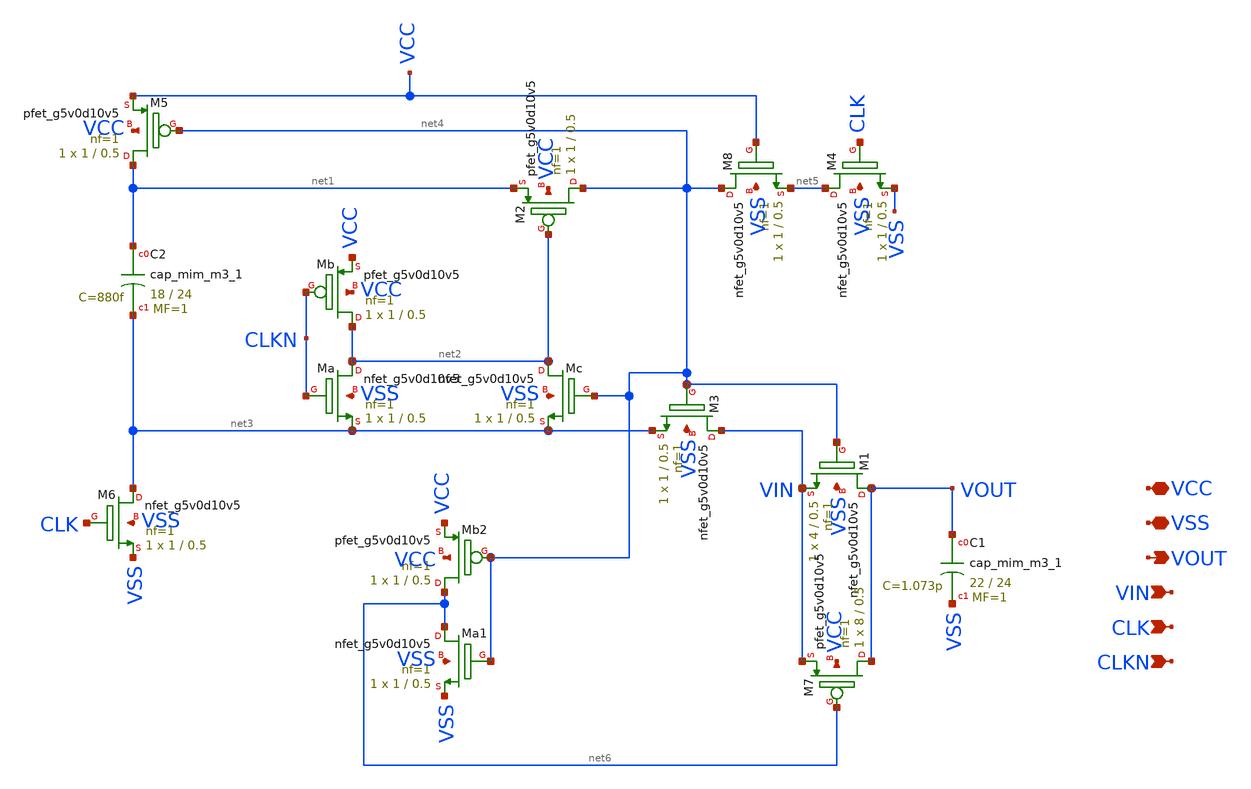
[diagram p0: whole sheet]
** sch_path: Sample&Hold/schematic/working/sample_hold.sch
**.subckt sample_hold VCC VIN VOUT CLK CLKN VSS
*.iopin VCC
*.ipin VIN
*.opin VOUT
*.ipin CLK
*.ipin CLKN
*.iopin VSS
XM5 net1 net4 VCC VCC sky130_fd_pr__pfet_g5v0d10v5 L=0.5 W=1 nf=1 ad='int((nf+1)/2) * W/nf * 0.29' as='int((nf+2)/2) * W/nf * 0.29'
+ pd='2*int((nf+1)/2) * (W/nf + 0.29)' ps='2*int((nf+2)/2) * (W/nf + 0.29)' nrd='0.29 / W' nrs='0.29 / W'
+ sa=0 sb=0 sd=0 mult=1 m=1
XM6 net3 CLK VSS VSS sky130_fd_pr__nfet_g5v0d10v5 L=0.5 W=1 nf=1 ad='int((nf+1)/2) * W/nf * 0.29' as='int((nf+2)/2) * W/nf * 0.29'
+ pd='2*int((nf+1)/2) * (W/nf + 0.29)' ps='2*int((nf+2)/2) * (W/nf + 0.29)' nrd='0.29 / W' nrs='0.29 / W'
+ sa=0 sb=0 sd=0 mult=1 m=1
XMa net2 CLKN net3 VSS sky130_fd_pr__nfet_g5v0d10v5 L=0.5 W=1 nf=1 ad='int((nf+1)/2) * W/nf * 0.29' as='int((nf+2)/2) * W/nf * 0.29'
+ pd='2*int((nf+1)/2) * (W/nf + 0.29)' ps='2*int((nf+2)/2) * (W/nf + 0.29)' nrd='0.29 / W' nrs='0.29 / W'
+ sa=0 sb=0 sd=0 mult=1 m=1
XMb net2 CLKN VCC VCC sky130_fd_pr__pfet_g5v0d10v5 L=0.5 W=1 nf=1 ad='int((nf+1)/2) * W/nf * 0.29' as='int((nf+2)/2) * W/nf * 0.29'
+ pd='2*int((nf+1)/2) * (W/nf + 0.29)' ps='2*int((nf+2)/2) * (W/nf + 0.29)' nrd='0.29 / W' nrs='0.29 / W'
+ sa=0 sb=0 sd=0 mult=1 m=1
XMc net2 net4 net3 VSS sky130_fd_pr__nfet_g5v0d10v5 L=0.5 W=1 nf=1 ad='int((nf+1)/2) * W/nf * 0.29' as='int((nf+2)/2) * W/nf * 0.29'
+ pd='2*int((nf+1)/2) * (W/nf + 0.29)' ps='2*int((nf+2)/2) * (W/nf + 0.29)' nrd='0.29 / W' nrs='0.29 / W'
+ sa=0 sb=0 sd=0 mult=1 m=1
XM2 net4 net2 net1 VCC sky130_fd_pr__pfet_g5v0d10v5 L=0.5 W=1 nf=1 ad='int((nf+1)/2) * W/nf * 0.29' as='int((nf+2)/2) * W/nf * 0.29'
+ pd='2*int((nf+1)/2) * (W/nf + 0.29)' ps='2*int((nf+2)/2) * (W/nf + 0.29)' nrd='0.29 / W' nrs='0.29 / W'
+ sa=0 sb=0 sd=0 mult=1 m=1
XM3 VIN net4 net3 VSS sky130_fd_pr__nfet_g5v0d10v5 L=0.5 W=1 nf=1 ad='int((nf+1)/2) * W/nf * 0.29' as='int((nf+2)/2) * W/nf * 0.29'
+ pd='2*int((nf+1)/2) * (W/nf + 0.29)' ps='2*int((nf+2)/2) * (W/nf + 0.29)' nrd='0.29 / W' nrs='0.29 / W'
+ sa=0 sb=0 sd=0 mult=1 m=1
XM8 net4 VCC net5 VSS sky130_fd_pr__nfet_g5v0d10v5 L=0.5 W=1 nf=1 ad='int((nf+1)/2) * W/nf * 0.29' as='int((nf+2)/2) * W/nf * 0.29'
+ pd='2*int((nf+1)/2) * (W/nf + 0.29)' ps='2*int((nf+2)/2) * (W/nf + 0.29)' nrd='0.29 / W' nrs='0.29 / W'
+ sa=0 sb=0 sd=0 mult=1 m=1
XM4 net5 CLK VSS VSS sky130_fd_pr__nfet_g5v0d10v5 L=0.5 W=1 nf=1 ad='int((nf+1)/2) * W/nf * 0.29' as='int((nf+2)/2) * W/nf * 0.29'
+ pd='2*int((nf+1)/2) * (W/nf + 0.29)' ps='2*int((nf+2)/2) * (W/nf + 0.29)' nrd='0.29 / W' nrs='0.29 / W'
+ sa=0 sb=0 sd=0 mult=1 m=1
XM1 VOUT net4 VIN VSS sky130_fd_pr__nfet_g5v0d10v5 L=0.5 W=4 nf=1 ad='int((nf+1)/2) * W/nf * 0.29' as='int((nf+2)/2) * W/nf * 0.29'
+ pd='2*int((nf+1)/2) * (W/nf + 0.29)' ps='2*int((nf+2)/2) * (W/nf + 0.29)' nrd='0.29 / W' nrs='0.29 / W'
+ sa=0 sb=0 sd=0 mult=1 m=1
XM7 VOUT net6 VIN VCC sky130_fd_pr__pfet_g5v0d10v5 L=0.5 W=8 nf=1 ad='int((nf+1)/2) * W/nf * 0.29' as='int((nf+2)/2) * W/nf * 0.29'
+ pd='2*int((nf+1)/2) * (W/nf + 0.29)' ps='2*int((nf+2)/2) * (W/nf + 0.29)' nrd='0.29 / W' nrs='0.29 / W'
+ sa=0 sb=0 sd=0 mult=1 m=1
XMa1 net6 net4 VSS VSS sky130_fd_pr__nfet_g5v0d10v5 L=0.5 W=1 nf=1 ad='int((nf+1)/2) * W/nf * 0.29' as='int((nf+2)/2) * W/nf * 0.29'
+ pd='2*int((nf+1)/2) * (W/nf + 0.29)' ps='2*int((nf+2)/2) * (W/nf + 0.29)' nrd='0.29 / W' nrs='0.29 / W'
+ sa=0 sb=0 sd=0 mult=1 m=1
XMb2 net6 net4 VCC VCC sky130_fd_pr__pfet_g5v0d10v5 L=0.5 W=1 nf=1 ad='int((nf+1)/2) * W/nf * 0.29' as='int((nf+2)/2) * W/nf * 0.29'
+ pd='2*int((nf+1)/2) * (W/nf + 0.29)' ps='2*int((nf+2)/2) * (W/nf + 0.29)' nrd='0.29 / W' nrs='0.29 / W'
+ sa=0 sb=0 sd=0 mult=1 m=1
XC1 VOUT VSS sky130_fd_pr__cap_mim_m3_1 W=22 L=24 MF=1 m=1
XC2 net1 net3 sky130_fd_pr__cap_mim_m3_1 W=18 L=24 MF=1 m=1
**.ends
.end
